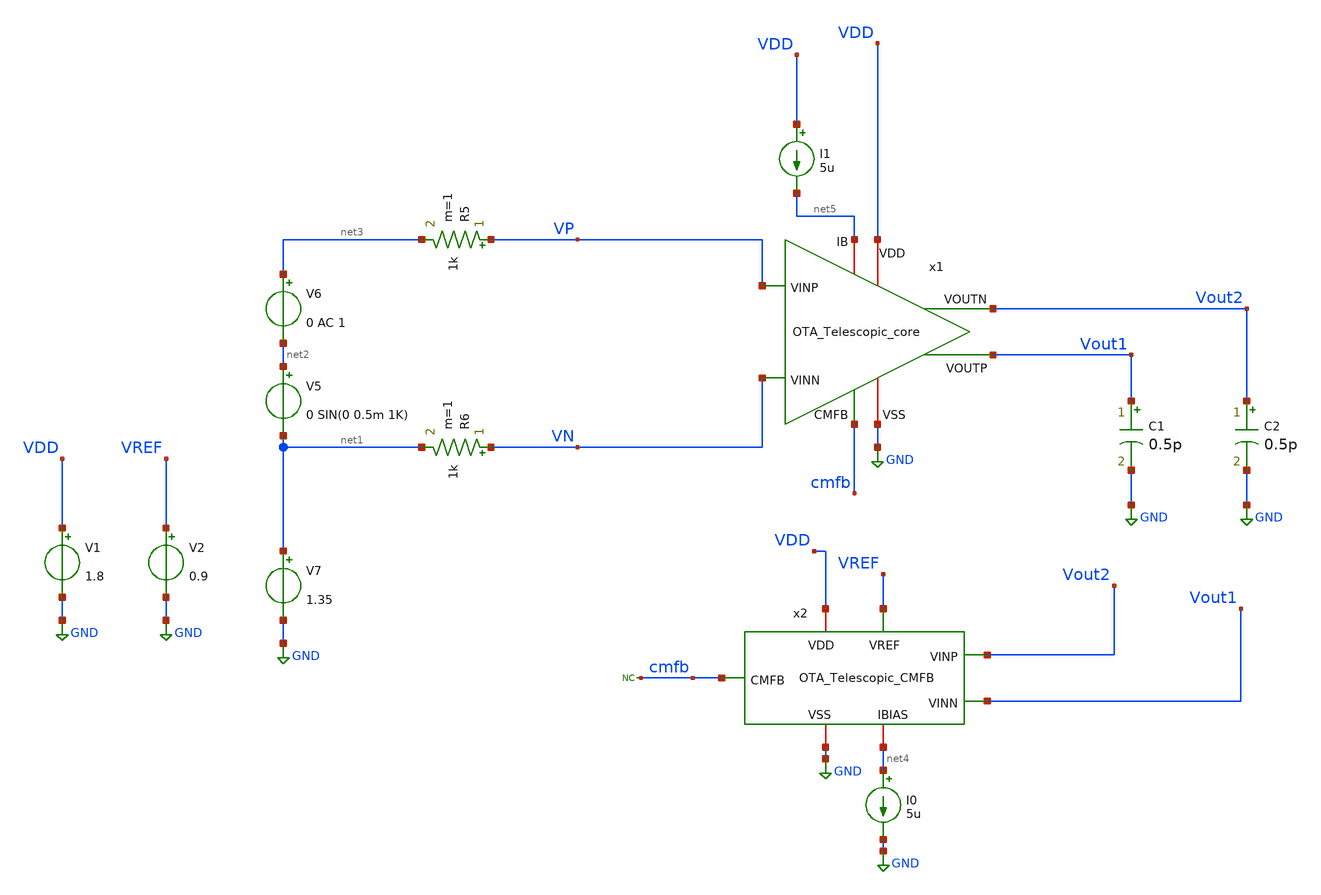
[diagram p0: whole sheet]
** sch_path: Differential_OTA_Telescopic_IHP/OTA_Telescopic_TB.sch
**.subckt OTA_Telescopic_TB
x1 VDD cmfb Vout1 Vout2 VP VN GND net5 OTA_Telescopic_core
V6 net3 net2 0 AC 1
V7 net1 GND 1.35
V5 net2 net1 0 SIN(0 0.5m 1K)
V1 VDD GND 1.8
V2 VREF GND 0.9
C1 Vout1 GND 0.5p m=1
C2 Vout2 GND 0.5p m=1
I0 net4 GND 5u
x2 VDD VREF Vout1 Vout2 net4 cmfb GND OTA_Telescopic_CMFB
R5 VP net3 1k m=1
R6 VN net1 1k m=1
* noconn cmfb
I1 VDD net5 5u
**** begin user architecture code

** opencircuitdesign pdks install
.lib $::SKYWATER_MODELS/sky130.lib.spice tt




.control
save all
 set color0 = white

* AC simulation
ac dec 10 1 1T
let Av = db(v(Vout1)-v(Vout2))
meas ac Ao MAX Av
let ABW = Ao-3
meas ac BW WHEN Av=ABW
meas ac UGBW WHEN Av=0
let phase_vec = 180/pi*cph(v(Vout1)-v(Vout2))

* Phase margin (PM)
meas ac phase FIND phase_vec WHEN frequency=UGBW
let PM = phase+180
print PM

* Gain margin (GM)
meas ac freq180 FIND frequency WHEN phase_vec=-180
meas ac gain FIND Av WHEN frequency=freq180
let GM = 0-gain
print GM
plot Av
plot phase_vec

write AC_OL.raw


*DC simulation

op
let vout_dc = v(Vout1)
print vout_dc
write OTA_Telescopic_TB.raw

.endc




.op

.save all
*OTA
.save @m.x1.xm1.msky130_fd_pr__nfet_01v8_lvt[id]
.save @m.x1.xm1.msky130_fd_pr__nfet_01v8_lvt[gm]
.save @m.x1.xm2.msky130_fd_pr__nfet_01v8_lvt[id]
.save @m.x1.xm2.msky130_fd_pr__nfet_01v8_lvt[gm]

.save @m.x1.xm9.msky130_fd_pr__pfet_01v8_lvt[id]
.save @m.x1.xm9.msky130_fd_pr__pfet_01v8_lvt[gm]
.save @m.x1.xm10.msky130_fd_pr__pfet_01v8_lvt[id]
.save @m.x1.xm10.msky130_fd_pr__pfet_01v8_lvt[gm]

.save @m.x1.xm0.msky130_fd_pr__nfet_01v8_lvt[id]

.save @m.x1.xm1.msky130_fd_pr__nfet_01v8_lvt[vdssat]


.save @m.x1.xm13.msky130_fd_pr__nfet_01v8_lvt[id]
.save @m.x1.xm14.msky130_fd_pr__nfet_01v8_lvt[id]
.save @m.x1.xm15.msky130_fd_pr__pfet_01v8_lvt[id]
.save @m.x1.xm16.msky130_fd_pr__nfet_01v8_lvt[id]
.save @m.x1.xm17.msky130_fd_pr__nfet_01v8_lvt[id]

.save @m.x1.xm18.msky130_fd_pr__pfet_01v8_lvt[id]
.save @m.x1.xm19.msky130_fd_pr__nfet_01v8_lvt[id]

*CMFB
.save @m.x2.xm0.msky130_fd_pr__pfet_01v8_lvt[id]
.save @m.x2.xm1.msky130_fd_pr__pfet_01v8_lvt[id]
.save @m.x2.xm1.msky130_fd_pr__pfet_01v8_lvt[gm]
.save @m.x2.xm2.msky130_fd_pr__pfet_01v8_lvt[id]
.save @m.x2.xm2.msky130_fd_pr__pfet_01v8_lvt[gm]
.save @m.x2.xm3.msky130_fd_pr__pfet_01v8_lvt[id]
.save @m.x2.xm3.msky130_fd_pr__pfet_01v8_lvt[gm]
.save @m.x2.xm4.msky130_fd_pr__pfet_01v8_lvt[id]
.save @m.x2.xm4.msky130_fd_pr__pfet_01v8_lvt[gm]
.save @m.x2.xm5.msky130_fd_pr__pfet_01v8_lvt[id]
.save @m.x2.xm5.msky130_fd_pr__pfet_01v8_lvt[gm]
.save @m.x2.xm6.msky130_fd_pr__pfet_01v8_lvt[id]
.save @m.x2.xm6.msky130_fd_pr__pfet_01v8_lvt[gm]

.save @m.x2.xm7.msky130_fd_pr__nfet_01v8_lvt[id]
.save @m.x2.xm7.msky130_fd_pr__nfet_01v8_lvt[gm]
.save @m.x2.xm8.msky130_fd_pr__nfet_01v8_lvt[id]
.save @m.x2.xm8.msky130_fd_pr__nfet_01v8_lvt[gm]



.control

let vdssat_M1 = @m.x1.xm1.msky130_fd_pr__nfet_01v8_lvt[vdsat]
let vdssat_M3 = @m.x1.xm3.msky130_fd_pr__nfet_01v8_lvt[vdsat]
let vdssat_M5 = @m.x1.xm5.msky130_fd_pr__pfet_01v8_lvt[vdsat]
let vdssat_M7 = @m.x1.xm7.msky130_fd_pr__pfet_01v8_lvt[vdsat]
let vdssat_M0 = @m.x1.xm0.msky130_fd_pr__nfet_01v8_lvt[vdsat]

print vdssat_M1
print vdssat_M3
print vdssat_M5
print vdssat_M7
print vdssat_M0

let ro_M1 = 1/@m.x1.xm1.msky130_fd_pr__nfet_01v8_lvt[gds]
let ro_M3 = 1/@m.x1.xm3.msky130_fd_pr__nfet_01v8_lvt[gds]
let ro_M5 = 1/@m.x1.xm5.msky130_fd_pr__pfet_01v8_lvt[gds]
let ro_M7 = 1/@m.x1.xm7.msky130_fd_pr__pfet_01v8_lvt[gds]
let ro_M0 = 1/@m.x1.xm0.msky130_fd_pr__nfet_01v8_lvt[gds]

print ro_M1
print ro_M3
print ro_M5
print ro_M7
print ro_M0

let gm_M1 = @m.x1.xm1.msky130_fd_pr__nfet_01v8_lvt[gm]
let gm_M3 = @m.x1.xm3.msky130_fd_pr__nfet_01v8_lvt[gm]
let gm_M5 = @m.x1.xm5.msky130_fd_pr__pfet_01v8_lvt[gm]
let gm_M7 = @m.x1.xm7.msky130_fd_pr__pfet_01v8_lvt[gm]
let gm_M0 = @m.x1.xm0.msky130_fd_pr__nfet_01v8_lvt[gm]

print gm_M1
print gm_M3
print gm_M5
print gm_M7
print gm_M0

let gmb_M3 = @m.x1.xm3.msky130_fd_pr__nfet_01v8_lvt[gmbs]
let gmb_M5 = @m.x1.xm5.msky130_fd_pr__pfet_01v8_lvt[gmbs]

print gmb_M3
print gmb_M5


*CMFB

let x2_vdssat_M0 = @m.x2.xm0.msky130_fd_pr__pfet_01v8_lvt[vdsat]
let x2_vth_M0 = @m.x2.xm0.msky130_fd_pr__pfet_01v8_lvt[vth]

print x2_vdssat_M0
print x2_vth_M0

.endc



**** end user architecture code
**.ends

* expanding   symbol:  OTA_Telescopic_core.sym # of pins=8
** sym_path: Differential_OTA_Telescopic_IHP/OTA_Telescopic_core.sym
** sch_path: Differential_OTA_Telescopic_IHP/OTA_Telescopic_core.sch
.subckt OTA_Telescopic_core VDD CMFB VOUTP VOUTN VINP VINN VSS IB
*.iopin VDD
*.iopin VSS
*.ipin VINP
*.ipin VINN
*.opin VOUTN
*.opin VOUTP
*.ipin CMFB
*.iopin IB
V2 VB2 VSS 1.6
V3 VB3 VSS 0.68
V4 VB4 VSS 0.49409
XM0 P CMFB VSS VSS sky130_fd_pr__nfet_01v8_lvt L=0.8 W=6 nf=1 ad='int((nf+1)/2) * W/nf * 0.29' as='int((nf+2)/2) * W/nf * 0.29'
+ pd='2*int((nf+1)/2) * (W/nf + 0.29)' ps='2*int((nf+2)/2) * (W/nf + 0.29)' nrd='0.29 / W' nrs='0.29 / W'
+ sa=0 sb=0 sd=0 mult=2*8*50 m=2*8*50
XM1 net2 VINP P VSS sky130_fd_pr__nfet_01v8_lvt L=0.15 W=1.2 nf=1 ad='int((nf+1)/2) * W/nf * 0.29' as='int((nf+2)/2) * W/nf * 0.29'
+ pd='2*int((nf+1)/2) * (W/nf + 0.29)' ps='2*int((nf+2)/2) * (W/nf + 0.29)' nrd='0.29 / W' nrs='0.29 / W'
+ sa=0 sb=0 sd=0 mult=1*50 m=1*50
XM2 net5 VINN P VSS sky130_fd_pr__nfet_01v8_lvt L=0.15 W=1.2 nf=1 ad='int((nf+1)/2) * W/nf * 0.29' as='int((nf+2)/2) * W/nf * 0.29'
+ pd='2*int((nf+1)/2) * (W/nf + 0.29)' ps='2*int((nf+2)/2) * (W/nf + 0.29)' nrd='0.29 / W' nrs='0.29 / W'
+ sa=0 sb=0 sd=0 mult=1*50 m=1*50
XM3 VE VB22 net2 VSS sky130_fd_pr__nfet_01v8_lvt L=0.15 W=2.5 nf=1 ad='int((nf+1)/2) * W/nf * 0.29' as='int((nf+2)/2) * W/nf * 0.29'
+ pd='2*int((nf+1)/2) * (W/nf + 0.29)' ps='2*int((nf+2)/2) * (W/nf + 0.29)' nrd='0.29 / W' nrs='0.29 / W'
+ sa=0 sb=0 sd=0 mult=1*50 m=1*50
XM4 net4 VB22 net5 VSS sky130_fd_pr__nfet_01v8_lvt L=0.15 W=2.5 nf=1 ad='int((nf+1)/2) * W/nf * 0.29'
+ as='int((nf+2)/2) * W/nf * 0.29' pd='2*int((nf+1)/2) * (W/nf + 0.29)' ps='2*int((nf+2)/2) * (W/nf + 0.29)'
+ nrd='0.29 / W' nrs='0.29 / W' sa=0 sb=0 sd=0 mult=1*50 m=1*50
XM5 VE VB33 net1 VDD sky130_fd_pr__pfet_01v8_lvt L=0.35 W=2 nf=1 ad='int((nf+1)/2) * W/nf * 0.29' as='int((nf+2)/2) * W/nf * 0.29'
+ pd='2*int((nf+1)/2) * (W/nf + 0.29)' ps='2*int((nf+2)/2) * (W/nf + 0.29)' nrd='0.29 / W' nrs='0.29 / W'
+ sa=0 sb=0 sd=0 mult=1*50 m=1*50
XM6 net4 VB33 net3 VDD sky130_fd_pr__pfet_01v8_lvt L=0.35 W=2 nf=1 ad='int((nf+1)/2) * W/nf * 0.29' as='int((nf+2)/2) * W/nf * 0.29'
+ pd='2*int((nf+1)/2) * (W/nf + 0.29)' ps='2*int((nf+2)/2) * (W/nf + 0.29)' nrd='0.29 / W' nrs='0.29 / W'
+ sa=0 sb=0 sd=0 mult=1*50 m=1*50
XM7 net1 VB55 VDD VDD sky130_fd_pr__pfet_01v8_lvt L=0.35 W=0.7 nf=1 ad='int((nf+1)/2) * W/nf * 0.29'
+ as='int((nf+2)/2) * W/nf * 0.29' pd='2*int((nf+1)/2) * (W/nf + 0.29)' ps='2*int((nf+2)/2) * (W/nf + 0.29)'
+ nrd='0.29 / W' nrs='0.29 / W' sa=0 sb=0 sd=0 mult=1*50 m=1*50
XM8 net3 VB55 VDD VDD sky130_fd_pr__pfet_01v8_lvt L=0.35 W=0.7 nf=1 ad='int((nf+1)/2) * W/nf * 0.29'
+ as='int((nf+2)/2) * W/nf * 0.29' pd='2*int((nf+1)/2) * (W/nf + 0.29)' ps='2*int((nf+2)/2) * (W/nf + 0.29)'
+ nrd='0.29 / W' nrs='0.29 / W' sa=0 sb=0 sd=0 mult=1*50 m=1*50
XM9 VOUTP VE VDD VDD sky130_fd_pr__pfet_01v8_lvt L=0.7 W=1.71 nf=1 ad='int((nf+1)/2) * W/nf * 0.29' as='int((nf+2)/2) * W/nf * 0.29'
+ pd='2*int((nf+1)/2) * (W/nf + 0.29)' ps='2*int((nf+2)/2) * (W/nf + 0.29)' nrd='0.29 / W' nrs='0.29 / W'
+ sa=0 sb=0 sd=0 mult=80 m=80
XM12 VOUTN IB VSS VSS sky130_fd_pr__nfet_01v8_lvt L=2.2 W=0.5 nf=1 ad='int((nf+1)/2) * W/nf * 0.29' as='int((nf+2)/2) * W/nf * 0.29'
+ pd='2*int((nf+1)/2) * (W/nf + 0.29)' ps='2*int((nf+2)/2) * (W/nf + 0.29)' nrd='0.29 / W' nrs='0.29 / W'
+ sa=0 sb=0 sd=0 mult=80 m=80
XM11 VOUTP IB VSS VSS sky130_fd_pr__nfet_01v8_lvt L=2.2 W=0.5 nf=1 ad='int((nf+1)/2) * W/nf * 0.29' as='int((nf+2)/2) * W/nf * 0.29'
+ pd='2*int((nf+1)/2) * (W/nf + 0.29)' ps='2*int((nf+2)/2) * (W/nf + 0.29)' nrd='0.29 / W' nrs='0.29 / W'
+ sa=0 sb=0 sd=0 mult=80 m=80
XM10 VOUTN net4 VDD VDD sky130_fd_pr__pfet_01v8_lvt L=0.7 W=1.71 nf=1 ad='int((nf+1)/2) * W/nf * 0.29'
+ as='int((nf+2)/2) * W/nf * 0.29' pd='2*int((nf+1)/2) * (W/nf + 0.29)' ps='2*int((nf+2)/2) * (W/nf + 0.29)'
+ nrd='0.29 / W' nrs='0.29 / W' sa=0 sb=0 sd=0 mult=80 m=80
XM13 IB IB VSS VSS sky130_fd_pr__nfet_01v8_lvt L=2.2 W=0.5 nf=1 ad='int((nf+1)/2) * W/nf * 0.29' as='int((nf+2)/2) * W/nf * 0.29'
+ pd='2*int((nf+1)/2) * (W/nf + 0.29)' ps='2*int((nf+2)/2) * (W/nf + 0.29)' nrd='0.29 / W' nrs='0.29 / W'
+ sa=0 sb=0 sd=0 mult=1 m=1
V1 VB5 VSS 0.7
XM14 VB55 IB VSS VSS sky130_fd_pr__nfet_01v8_lvt L=2.2 W=0.5 nf=1 ad='int((nf+1)/2) * W/nf * 0.29' as='int((nf+2)/2) * W/nf * 0.29'
+ pd='2*int((nf+1)/2) * (W/nf + 0.29)' ps='2*int((nf+2)/2) * (W/nf + 0.29)' nrd='0.29 / W' nrs='0.29 / W'
+ sa=0 sb=0 sd=0 mult=4 m=4
XM15 VB55 VB55 VDD VDD sky130_fd_pr__pfet_01v8_lvt L=0.37 W=0.45 nf=1 ad='int((nf+1)/2) * W/nf * 0.29'
+ as='int((nf+2)/2) * W/nf * 0.29' pd='2*int((nf+1)/2) * (W/nf + 0.29)' ps='2*int((nf+2)/2) * (W/nf + 0.29)'
+ nrd='0.29 / W' nrs='0.29 / W' sa=0 sb=0 sd=0 mult=1 m=1
XM16 VB33 IB VSS VSS sky130_fd_pr__nfet_01v8_lvt L=2.2 W=0.5 nf=1 ad='int((nf+1)/2) * W/nf * 0.29' as='int((nf+2)/2) * W/nf * 0.29'
+ pd='2*int((nf+1)/2) * (W/nf + 0.29)' ps='2*int((nf+2)/2) * (W/nf + 0.29)' nrd='0.29 / W' nrs='0.29 / W'
+ sa=0 sb=0 sd=0 mult=4 m=4
XM17 VB33 VB33 VDD VDD sky130_fd_pr__pfet_01v8_lvt L=0.42 W=0.51 nf=1 ad='int((nf+1)/2) * W/nf * 0.29'
+ as='int((nf+2)/2) * W/nf * 0.29' pd='2*int((nf+1)/2) * (W/nf + 0.29)' ps='2*int((nf+2)/2) * (W/nf + 0.29)'
+ nrd='0.29 / W' nrs='0.29 / W' sa=0 sb=0 sd=0 mult=1 m=1
XM18 VB22 VB33 VDD VDD sky130_fd_pr__pfet_01v8_lvt L=0.42 W=0.51 nf=1 ad='int((nf+1)/2) * W/nf * 0.29'
+ as='int((nf+2)/2) * W/nf * 0.29' pd='2*int((nf+1)/2) * (W/nf + 0.29)' ps='2*int((nf+2)/2) * (W/nf + 0.29)'
+ nrd='0.29 / W' nrs='0.29 / W' sa=0 sb=0 sd=0 mult=1 m=1
XM19 VB22 VB22 VSS VSS sky130_fd_pr__nfet_01v8_lvt L=8 W=0.5 nf=1 ad='int((nf+1)/2) * W/nf * 0.29' as='int((nf+2)/2) * W/nf * 0.29'
+ pd='2*int((nf+1)/2) * (W/nf + 0.29)' ps='2*int((nf+2)/2) * (W/nf + 0.29)' nrd='0.29 / W' nrs='0.29 / W'
+ sa=0 sb=0 sd=0 mult=1 m=1
* noconn VB2
* noconn VB3
* noconn VB4
* noconn VB5
V5 VB VSS 0.90204
* noconn VB
R1 net6 VOUTP 1 m=1
R2 VOUTN net7 1 m=1
C1 VE net6 0.1p m=1
C2 net7 net4 0.1p m=1
.ends


* expanding   symbol:  OTA_Telescopic_CMFB.sym # of pins=7
** sym_path: Differential_OTA_Telescopic_IHP/OTA_Telescopic_CMFB.sym
** sch_path: Differential_OTA_Telescopic_IHP/OTA_Telescopic_CMFB.sch
.subckt OTA_Telescopic_CMFB VDD VREF VINN VINP IBIAS CMFB VSS
*.iopin VDD
*.iopin VSS
*.opin CMFB
*.ipin VREF
*.iopin IBIAS
*.ipin VINP
*.ipin VINN
XM0 IBIAS IBIAS VDD VDD sky130_fd_pr__pfet_01v8_lvt L=0.85 W=15 nf=1 ad='int((nf+1)/2) * W/nf * 0.29'
+ as='int((nf+2)/2) * W/nf * 0.29' pd='2*int((nf+1)/2) * (W/nf + 0.29)' ps='2*int((nf+2)/2) * (W/nf + 0.29)'
+ nrd='0.29 / W' nrs='0.29 / W' sa=0 sb=0 sd=0 mult=1 m=1
XM7 net1 net1 VSS VSS sky130_fd_pr__nfet_01v8_lvt L=0.8 W=6 nf=1 ad='int((nf+1)/2) * W/nf * 0.29' as='int((nf+2)/2) * W/nf * 0.29'
+ pd='2*int((nf+1)/2) * (W/nf + 0.29)' ps='2*int((nf+2)/2) * (W/nf + 0.29)' nrd='0.29 / W' nrs='0.29 / W'
+ sa=0 sb=0 sd=0 mult=2 m=2
XM4 net1 VREF V1 VDD sky130_fd_pr__pfet_01v8_lvt L=0.35 W=20 nf=1 ad='int((nf+1)/2) * W/nf * 0.29' as='int((nf+2)/2) * W/nf * 0.29'
+ pd='2*int((nf+1)/2) * (W/nf + 0.29)' ps='2*int((nf+2)/2) * (W/nf + 0.29)' nrd='0.29 / W' nrs='0.29 / W'
+ sa=0 sb=0 sd=0 mult=1 m=1
XM5 net1 VREF V2 VDD sky130_fd_pr__pfet_01v8_lvt L=0.35 W=20 nf=1 ad='int((nf+1)/2) * W/nf * 0.29' as='int((nf+2)/2) * W/nf * 0.29'
+ pd='2*int((nf+1)/2) * (W/nf + 0.29)' ps='2*int((nf+2)/2) * (W/nf + 0.29)' nrd='0.29 / W' nrs='0.29 / W'
+ sa=0 sb=0 sd=0 mult=1 m=1
XM3 CMFB VINP V1 VDD sky130_fd_pr__pfet_01v8_lvt L=0.35 W=20 nf=1 ad='int((nf+1)/2) * W/nf * 0.29' as='int((nf+2)/2) * W/nf * 0.29'
+ pd='2*int((nf+1)/2) * (W/nf + 0.29)' ps='2*int((nf+2)/2) * (W/nf + 0.29)' nrd='0.29 / W' nrs='0.29 / W'
+ sa=0 sb=0 sd=0 mult=1 m=1
XM6 CMFB VINN V2 VDD sky130_fd_pr__pfet_01v8_lvt L=0.35 W=20 nf=1 ad='int((nf+1)/2) * W/nf * 0.29' as='int((nf+2)/2) * W/nf * 0.29'
+ pd='2*int((nf+1)/2) * (W/nf + 0.29)' ps='2*int((nf+2)/2) * (W/nf + 0.29)' nrd='0.29 / W' nrs='0.29 / W'
+ sa=0 sb=0 sd=0 mult=1 m=1
XM1 V1 IBIAS VDD VDD sky130_fd_pr__pfet_01v8_lvt L=0.85 W=15 nf=1 ad='int((nf+1)/2) * W/nf * 0.29' as='int((nf+2)/2) * W/nf * 0.29'
+ pd='2*int((nf+1)/2) * (W/nf + 0.29)' ps='2*int((nf+2)/2) * (W/nf + 0.29)' nrd='0.29 / W' nrs='0.29 / W'
+ sa=0 sb=0 sd=0 mult=1 m=1
XM2 V2 IBIAS VDD VDD sky130_fd_pr__pfet_01v8_lvt L=0.85 W=15 nf=1 ad='int((nf+1)/2) * W/nf * 0.29' as='int((nf+2)/2) * W/nf * 0.29'
+ pd='2*int((nf+1)/2) * (W/nf + 0.29)' ps='2*int((nf+2)/2) * (W/nf + 0.29)' nrd='0.29 / W' nrs='0.29 / W'
+ sa=0 sb=0 sd=0 mult=1 m=1
XM8 CMFB CMFB VSS VSS sky130_fd_pr__nfet_01v8_lvt L=0.8 W=6 nf=1 ad='int((nf+1)/2) * W/nf * 0.29' as='int((nf+2)/2) * W/nf * 0.29'
+ pd='2*int((nf+1)/2) * (W/nf + 0.29)' ps='2*int((nf+2)/2) * (W/nf + 0.29)' nrd='0.29 / W' nrs='0.29 / W'
+ sa=0 sb=0 sd=0 mult=2 m=2
.ends

.GLOBAL GND
.end
